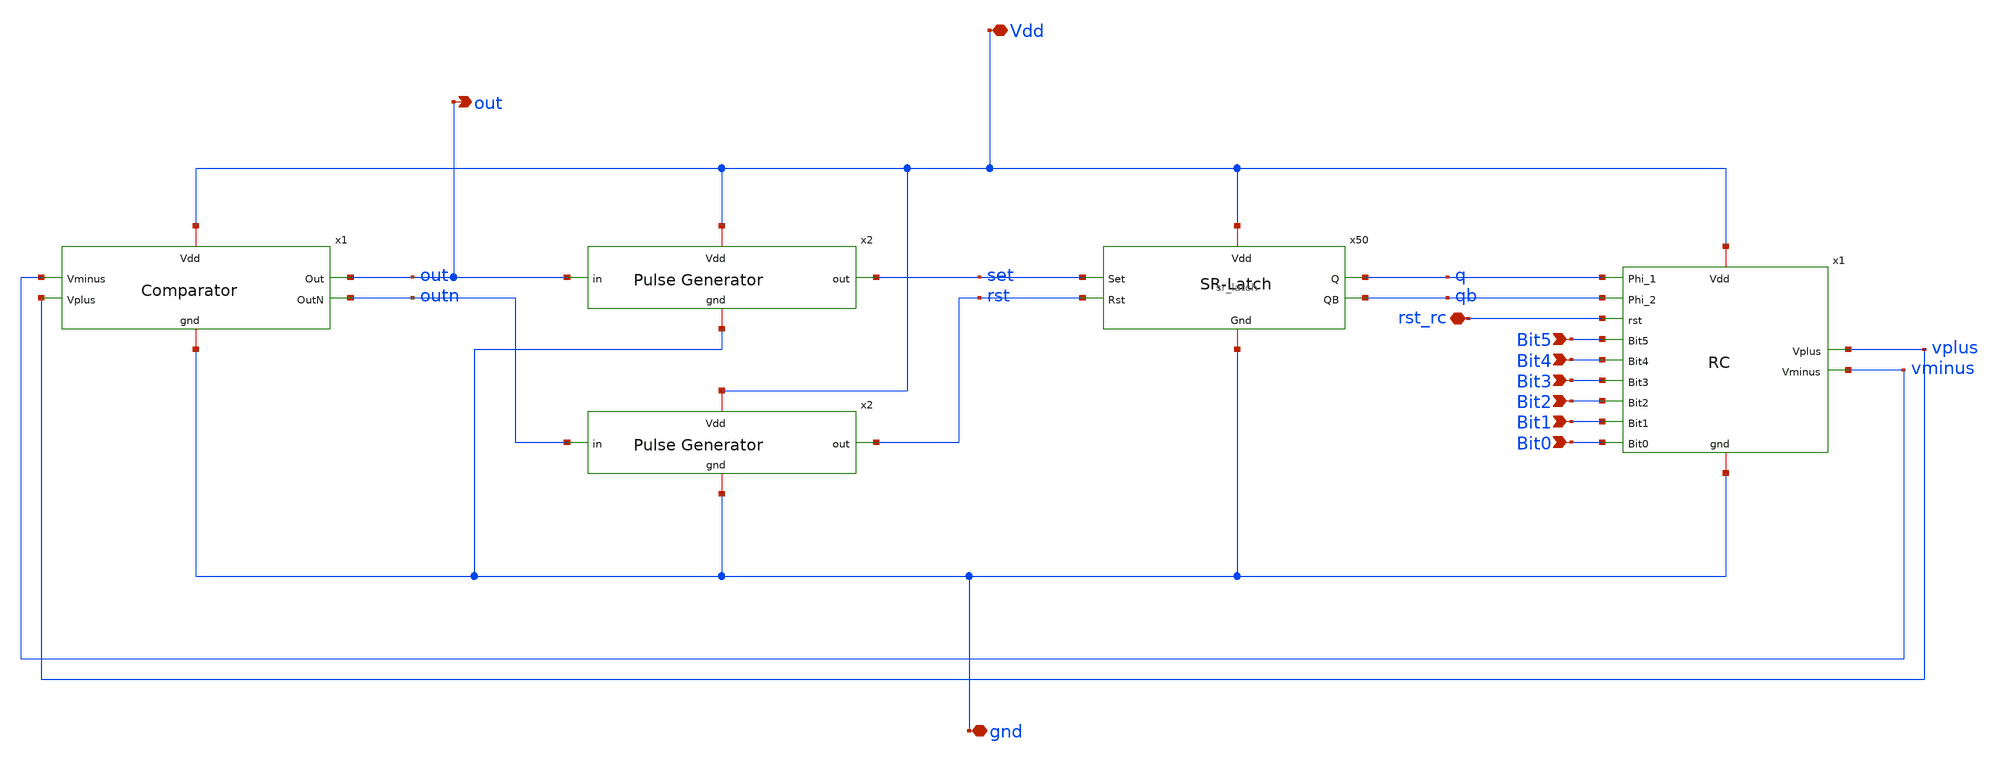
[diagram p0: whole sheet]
** sch_path: xschem/relax_oscillator_tb.sch
**.subckt relax_oscillator_tb Vdd gnd Bit5 Bit4 Bit3 Bit2 Bit1 Bit0 out rst_rc
*.iopin Vdd
*.iopin gnd
*.ipin Bit5
*.ipin Bit4
*.ipin Bit3
*.ipin Bit2
*.ipin Bit1
*.ipin Bit0
*.opin out
*.iopin rst_rc
x1 Vdd out outn vminus vplus gnd comparator
x2 Vdd set out gnd pulse_generator
x3 Vdd rst outn gnd pulse_generator
x4 Vdd set rst q qb gnd sr_latch
x5 Vdd q qb rst_rc vplus vminus Bit4 Bit0 Bit3 Bit2 Bit1 Bit5 gnd rc
**.ends
.end
